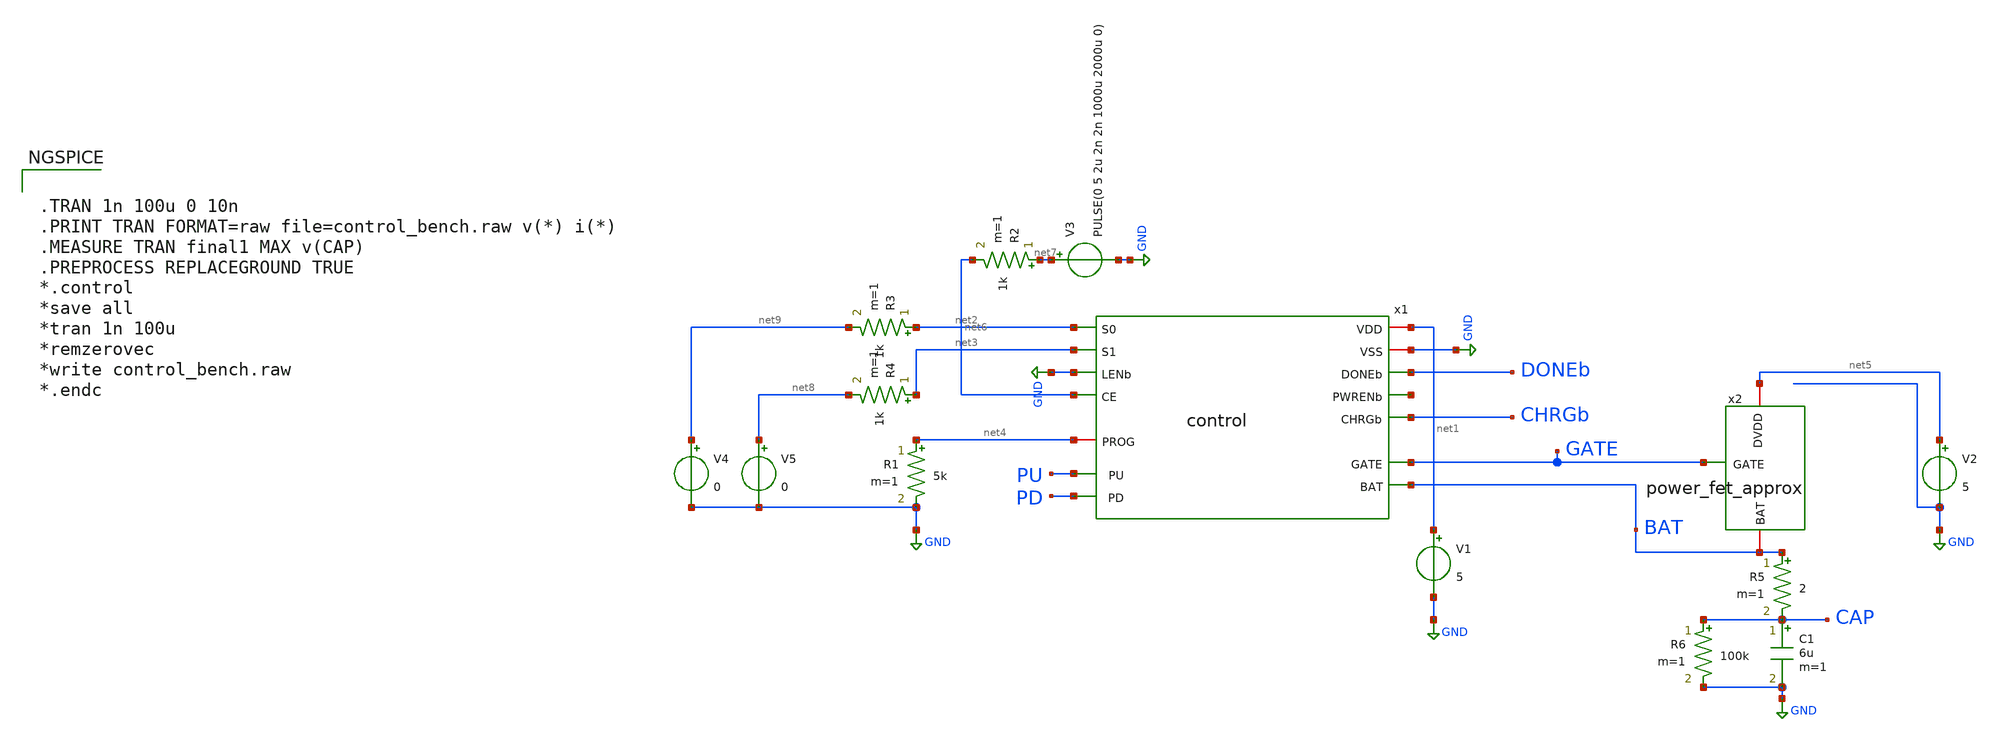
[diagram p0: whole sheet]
** sch_path: analog/xschem/control_bench.sch
**.subckt control_bench
x1 net1 GND net2 DONEb net3 GND net10 net6 BAT CHRGb net4 GATE PU PD control
V1 net1 GND 5
R1 net4 GND 5k m=1
R2 net7 net6 1k m=1
V2 net5 GND 5
R3 net2 net9 1k m=1
R4 net3 net8 1k m=1
V3 net7 GND PULSE(0 5 2u 2n 2n 1000u 2000u 0)
C1 CAP GND 6u m=1
R5 BAT CAP 2 m=1
R6 CAP GND 100k m=1
x2 net5 GATE BAT power_fet_approx
V4 net9 GND 0
V5 net8 GND 0
**** begin user architecture code


.TRAN 1n 100u 0 10n
.PRINT TRAN FORMAT=raw file=control_bench.raw v(*) i(*)
.MEASURE TRAN final1 MAX v(CAP)
.PREPROCESS REPLACEGROUND TRUE
*.control
*save all
*tran 1n 100u
*remzerovec
*write control_bench.raw
*.endc



.include $::PDK_ROOT/gf180mcuD/libs.tech/xyce/design.xyce
.lib $::PDK_ROOT/gf180mcuD/libs.tech/xyce/sm141064.xyce typical
.lib $::PDK_ROOT/gf180mcuD/libs.tech/xyce/sm141064.xyce res_typical
.lib $::PDK_ROOT/gf180mcuD/libs.tech/xyce/sm141064.xyce diode_typical
.lib $::PDK_ROOT/gf180mcuD/libs.tech/xyce/sm141064.xyce mimcap_typical
.lib $::PDK_ROOT/gf180mcuD/libs.tech/xyce/sm141064.xyce cap_mim
.include /foss/designs/charger/xschem/extracted/power_fet_f.spice

**** end user architecture code
**.ends
.GLOBAL GND
.end
